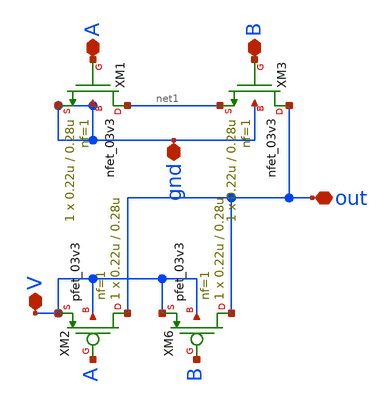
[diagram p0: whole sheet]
** sch_path: xschem/nand_gate.sch
**.subckt nand_gate A out gnd V B
*.iopin A
*.iopin out
*.iopin gnd
*.iopin V
*.iopin B
XM6 out B V V pfet_03v3 L=0.28u W=0.22u nf=1 ad='int((nf+1)/2) * W/nf * 0.18u' as='int((nf+2)/2) * W/nf * 0.18u'
+ pd='2*int((nf+1)/2) * (W/nf + 0.18u)' ps='2*int((nf+2)/2) * (W/nf + 0.18u)' nrd='0.18u / W' nrs='0.18u / W'
+ sa=0 sb=0 sd=0 m=1
XM1 net1 A gnd gnd nfet_03v3 L=0.28u W=0.22u nf=1 ad='int((nf+1)/2) * W/nf * 0.18u' as='int((nf+2)/2) * W/nf * 0.18u'
+ pd='2*int((nf+1)/2) * (W/nf + 0.18u)' ps='2*int((nf+2)/2) * (W/nf + 0.18u)' nrd='0.18u / W' nrs='0.18u / W'
+ sa=0 sb=0 sd=0 m=1
XM3 out B net1 gnd nfet_03v3 L=0.28u W=0.22u nf=1 ad='int((nf+1)/2) * W/nf * 0.18u' as='int((nf+2)/2) * W/nf * 0.18u'
+ pd='2*int((nf+1)/2) * (W/nf + 0.18u)' ps='2*int((nf+2)/2) * (W/nf + 0.18u)' nrd='0.18u / W' nrs='0.18u / W'
+ sa=0 sb=0 sd=0 m=1
XM2 out A V V pfet_03v3 L=0.28u W=0.22u nf=1 ad='int((nf+1)/2) * W/nf * 0.18u' as='int((nf+2)/2) * W/nf * 0.18u'
+ pd='2*int((nf+1)/2) * (W/nf + 0.18u)' ps='2*int((nf+2)/2) * (W/nf + 0.18u)' nrd='0.18u / W' nrs='0.18u / W'
+ sa=0 sb=0 sd=0 m=1
**.ends
.end
